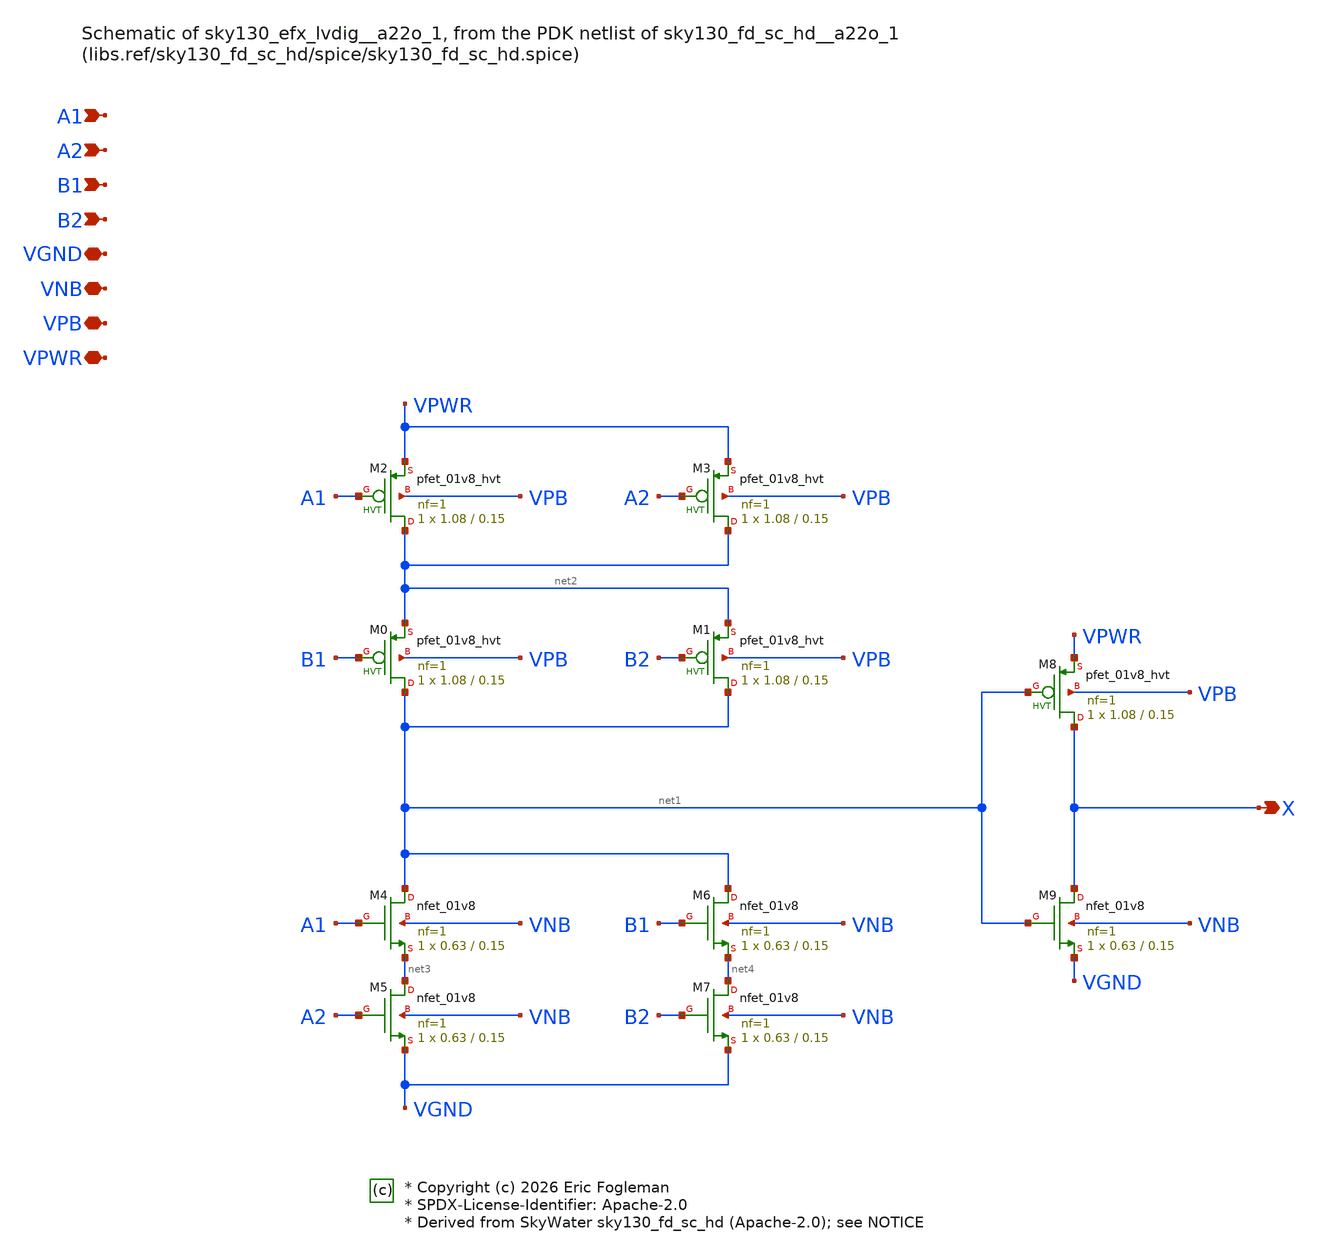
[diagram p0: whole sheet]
** sch_path: xschem/sky130_efx_lvdig__a22o_1.sch

* Copyright (c) 2026 Eric Fogleman
* SPDX-License-Identifier: Apache-2.0
* Derived from SkyWater sky130_fd_sc_hd (Apache-2.0); see NOTICE

**.subckt sky130_efx_lvdig__a22o_1 X A1 A2 B1 B2 VGND VNB VPB VPWR
*.opin X
*.ipin A1
*.ipin A2
*.ipin B1
*.ipin B2
*.iopin VGND
*.iopin VNB
*.iopin VPB
*.iopin VPWR
XM0 net1 B1 net2 VPB sky130_fd_pr__pfet_01v8_hvt L=0.15 W=1.08 nf=1 ad='int((1 + 1)/2) * 1.08 / 1 * 0.29'
+ as='int((1 + 2)/2) * 1.08 / 1 * 0.29' pd='2*int((1 + 1)/2) * (1.08 / 1 + 0.29)' ps='2*int((1 + 2)/2) * (1.08 / 1 + 0.29)'
+ nrd='0.29 / 1.08 ' nrs='0.29 / 1.08 ' sa=0 sb=0 sd=0 mult=1 m=1
XM1 net1 B2 net2 VPB sky130_fd_pr__pfet_01v8_hvt L=0.15 W=1.08 nf=1 ad='int((1 + 1)/2) * 1.08 / 1 * 0.29'
+ as='int((1 + 2)/2) * 1.08 / 1 * 0.29' pd='2*int((1 + 1)/2) * (1.08 / 1 + 0.29)' ps='2*int((1 + 2)/2) * (1.08 / 1 + 0.29)'
+ nrd='0.29 / 1.08 ' nrs='0.29 / 1.08 ' sa=0 sb=0 sd=0 mult=1 m=1
XM2 net2 A1 VPWR VPB sky130_fd_pr__pfet_01v8_hvt L=0.15 W=1.08 nf=1 ad='int((1 + 1)/2) * 1.08 / 1 * 0.29'
+ as='int((1 + 2)/2) * 1.08 / 1 * 0.29' pd='2*int((1 + 1)/2) * (1.08 / 1 + 0.29)' ps='2*int((1 + 2)/2) * (1.08 / 1 + 0.29)'
+ nrd='0.29 / 1.08 ' nrs='0.29 / 1.08 ' sa=0 sb=0 sd=0 mult=1 m=1
XM3 net2 A2 VPWR VPB sky130_fd_pr__pfet_01v8_hvt L=0.15 W=1.08 nf=1 ad='int((1 + 1)/2) * 1.08 / 1 * 0.29'
+ as='int((1 + 2)/2) * 1.08 / 1 * 0.29' pd='2*int((1 + 1)/2) * (1.08 / 1 + 0.29)' ps='2*int((1 + 2)/2) * (1.08 / 1 + 0.29)'
+ nrd='0.29 / 1.08 ' nrs='0.29 / 1.08 ' sa=0 sb=0 sd=0 mult=1 m=1
XM4 net1 A1 net3 VNB sky130_fd_pr__nfet_01v8 L=0.15 W=0.63 nf=1 ad='int((1 + 1)/2) * 0.63 / 1 * 0.29'
+ as='int((1 + 2)/2) * 0.63 / 1 * 0.29' pd='2*int((1 + 1)/2) * (0.63 / 1 + 0.29)' ps='2*int((1 + 2)/2) * (0.63 / 1 + 0.29)'
+ nrd='0.29 / 0.63 ' nrs='0.29 / 0.63 ' sa=0 sb=0 sd=0 mult=1 m=1
XM5 net3 A2 VGND VNB sky130_fd_pr__nfet_01v8 L=0.15 W=0.63 nf=1 ad='int((1 + 1)/2) * 0.63 / 1 * 0.29'
+ as='int((1 + 2)/2) * 0.63 / 1 * 0.29' pd='2*int((1 + 1)/2) * (0.63 / 1 + 0.29)' ps='2*int((1 + 2)/2) * (0.63 / 1 + 0.29)'
+ nrd='0.29 / 0.63 ' nrs='0.29 / 0.63 ' sa=0 sb=0 sd=0 mult=1 m=1
XM6 net1 B1 net4 VNB sky130_fd_pr__nfet_01v8 L=0.15 W=0.63 nf=1 ad='int((1 + 1)/2) * 0.63 / 1 * 0.29'
+ as='int((1 + 2)/2) * 0.63 / 1 * 0.29' pd='2*int((1 + 1)/2) * (0.63 / 1 + 0.29)' ps='2*int((1 + 2)/2) * (0.63 / 1 + 0.29)'
+ nrd='0.29 / 0.63 ' nrs='0.29 / 0.63 ' sa=0 sb=0 sd=0 mult=1 m=1
XM7 net4 B2 VGND VNB sky130_fd_pr__nfet_01v8 L=0.15 W=0.63 nf=1 ad='int((1 + 1)/2) * 0.63 / 1 * 0.29'
+ as='int((1 + 2)/2) * 0.63 / 1 * 0.29' pd='2*int((1 + 1)/2) * (0.63 / 1 + 0.29)' ps='2*int((1 + 2)/2) * (0.63 / 1 + 0.29)'
+ nrd='0.29 / 0.63 ' nrs='0.29 / 0.63 ' sa=0 sb=0 sd=0 mult=1 m=1
XM8 X net1 VPWR VPB sky130_fd_pr__pfet_01v8_hvt L=0.15 W=1.08 nf=1 ad='int((1 + 1)/2) * 1.08 / 1 * 0.29'
+ as='int((1 + 2)/2) * 1.08 / 1 * 0.29' pd='2*int((1 + 1)/2) * (1.08 / 1 + 0.29)' ps='2*int((1 + 2)/2) * (1.08 / 1 + 0.29)'
+ nrd='0.29 / 1.08 ' nrs='0.29 / 1.08 ' sa=0 sb=0 sd=0 mult=1 m=1
XM9 X net1 VGND VNB sky130_fd_pr__nfet_01v8 L=0.15 W=0.63 nf=1 ad='int((1 + 1)/2) * 0.63 / 1 * 0.29'
+ as='int((1 + 2)/2) * 0.63 / 1 * 0.29' pd='2*int((1 + 1)/2) * (0.63 / 1 + 0.29)' ps='2*int((1 + 2)/2) * (0.63 / 1 + 0.29)'
+ nrd='0.29 / 0.63 ' nrs='0.29 / 0.63 ' sa=0 sb=0 sd=0 mult=1 m=1
**.ends
.end
